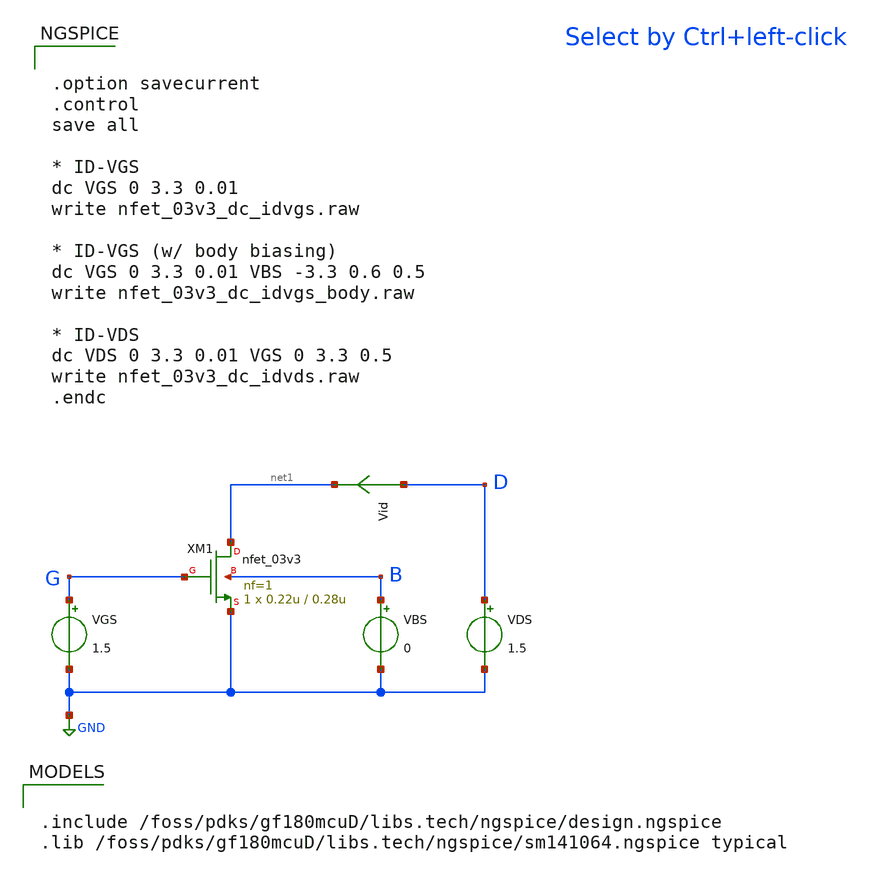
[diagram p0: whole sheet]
** sch_path: mosfet_gf180/nfet_03v3_dc.sch
**.subckt nfet_03v3_dc
XM1 net1 G GND B nfet_03v3 L=0.28u W=0.22u nf=1 ad='int((nf+1)/2) * W/nf * 0.18u' as='int((nf+2)/2) * W/nf * 0.18u'
+ pd='2*int((nf+1)/2) * (W/nf + 0.18u)' ps='2*int((nf+2)/2) * (W/nf + 0.18u)' nrd='0.18u / W' nrs='0.18u / W'
+ sa=0 sb=0 sd=0 m=1
VBS B GND 0
VGS G GND 1.5
VDS D GND 1.5
Vid D net1 0
.save i(vid)
**** begin user architecture code

.include /foss/pdks/gf180mcuD/libs.tech/ngspice/design.ngspice
.lib /foss/pdks/gf180mcuD/libs.tech/ngspice/sm141064.ngspice typical


.option savecurrent
.control
save all

* ID-VGS
dc VGS 0 3.3 0.01
write nfet_03v3_dc_idvgs.raw

* ID-VGS (w/ body biasing)
dc VGS 0 3.3 0.01 VBS -3.3 0.6 0.5
write nfet_03v3_dc_idvgs_body.raw

* ID-VDS
dc VDS 0 3.3 0.01 VGS 0 3.3 0.5
write nfet_03v3_dc_idvds.raw
.endc

**** end user architecture code
**.ends
.GLOBAL GND
.end
